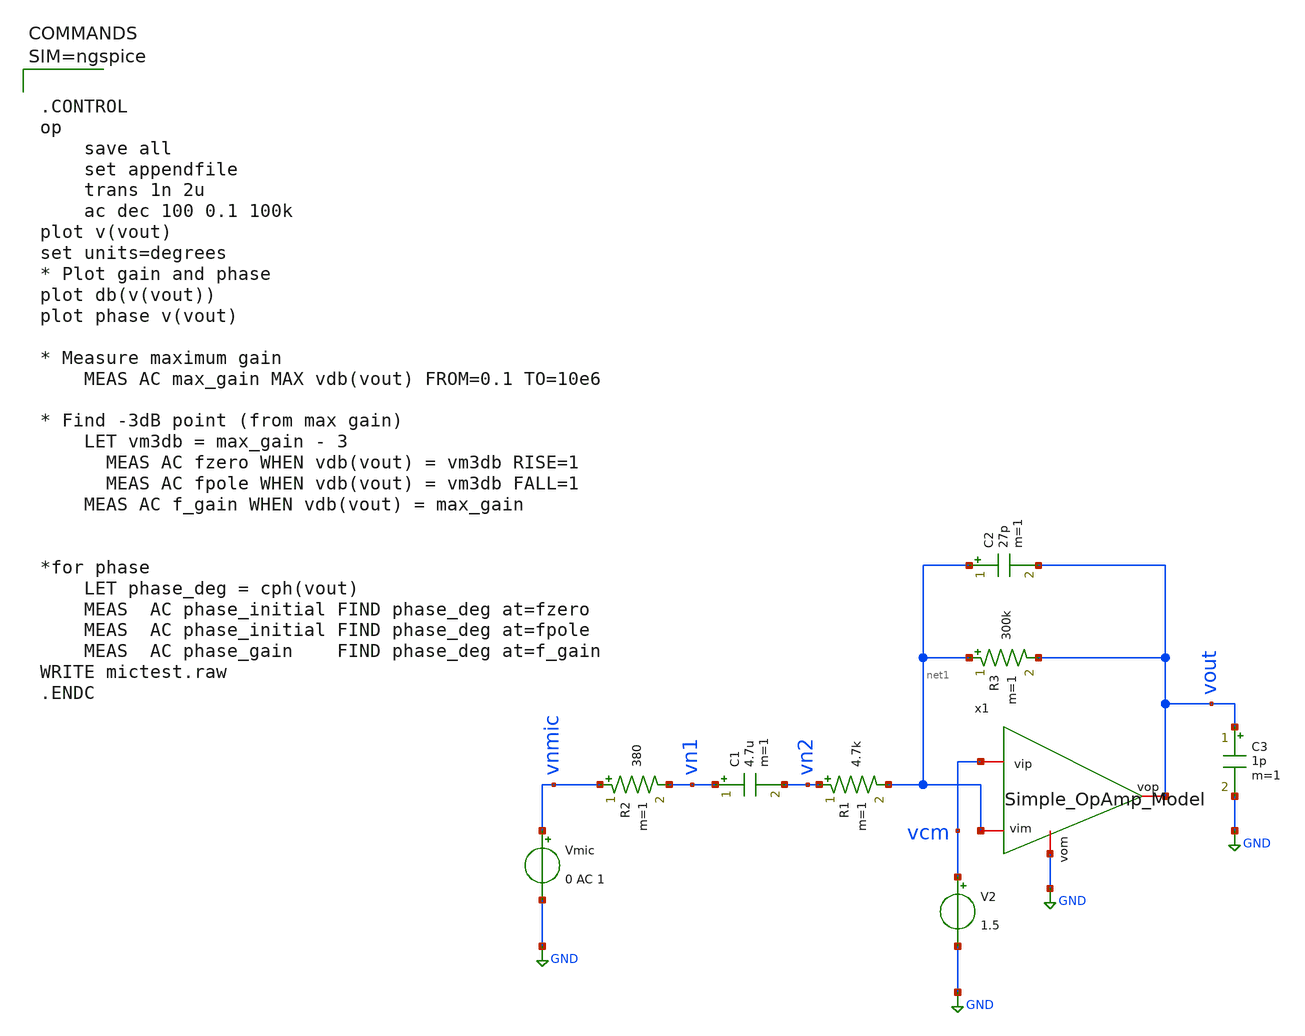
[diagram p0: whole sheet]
** sch_path: work/xschem/mictest_opamp.sch
**.subckt mictest_opamp
Vmic vnmic GND 0 AC 1
R2 vnmic vn1 380 m=1
C1 vn1 vn2 4.7u m=1
R1 vn2 net1 4.7k m=1
R3 net1 vout 300k m=1
C2 net1 vout 27p m=1
V2 vcm GND 1.5
C3 vout GND 1p m=1
x1 vout vcm net1 GND Simple_OpAmp_Model
**** begin user architecture code



.CONTROL
op
	save all
	set appendfile
	trans 1n 2u
	ac dec 100 0.1 100k
plot v(vout)
set units=degrees
* Plot gain and phase
plot db(v(vout))
plot phase v(vout)

* Measure maximum gain
	MEAS AC max_gain MAX vdb(vout) FROM=0.1 TO=10e6

* Find -3dB point (from max gain)
	LET vm3db = max_gain - 3
  	MEAS AC fzero WHEN vdb(vout) = vm3db RISE=1
  	MEAS AC fpole WHEN vdb(vout) = vm3db FALL=1
	MEAS AC f_gain WHEN vdb(vout) = max_gain


*for phase
	LET phase_deg = cph(vout)
	MEAS  AC phase_initial FIND phase_deg at=fzero
	MEAS  AC phase_initial FIND phase_deg at=fpole
	MEAS  AC phase_gain    FIND phase_deg at=f_gain
WRITE mictest.raw
.ENDC



**** end user architecture code
**.ends

* expanding   symbol:  Simple_OpAmp_Model.sym # of pins=4
** sym_path: work/xschem/Simple_OpAmp_Model.sym
** sch_path: work/xschem/Simple_OpAmp_Model.sch
.subckt Simple_OpAmp_Model vop vip vim vom
*.iopin vop
*.iopin vom
*.iopin vim
*.iopin vip
E1 vop vom vip vim 1000
.ends

.GLOBAL GND
.end
